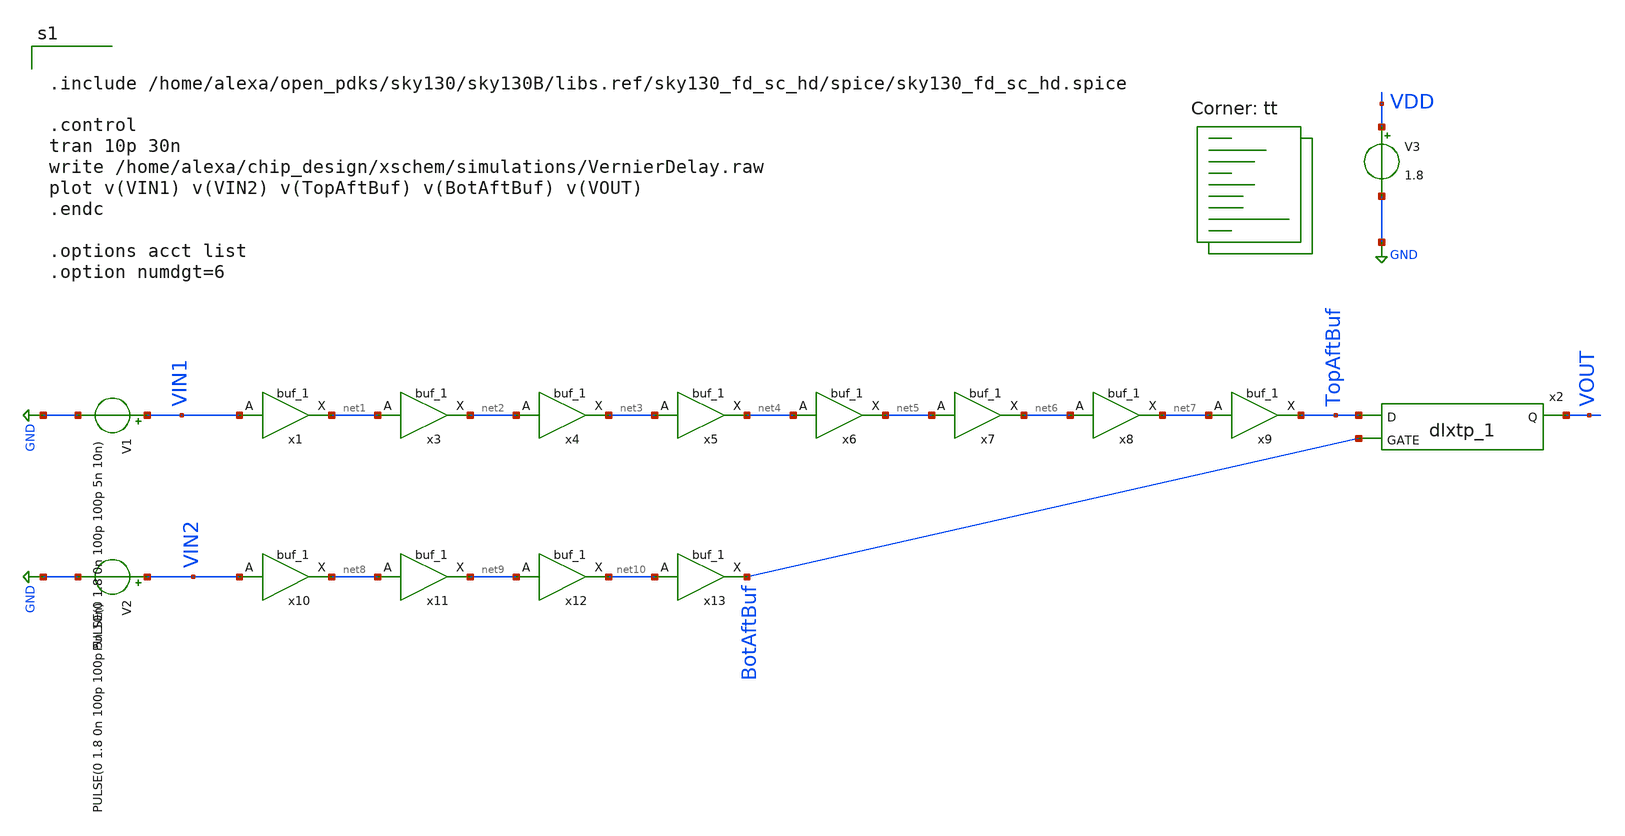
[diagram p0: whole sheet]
** sch_path: xschem/projects/SingleVernier.sch
* Copyright 2021 Stefan Frederik Schippers
* Licensed under the Apache License, Version 2.0 (the "License");
* you may not use this file except in compliance with the License.
* You may obtain a copy of the License at
* https://www.apache.org/licenses/LICENSE-2.0
* Unless required by applicable law or agreed to in writing, software
* distributed under the License is distributed on an "AS IS" BASIS,
* WITHOUT WARRANTIES OR CONDITIONS OF ANY KIND, either express or implied.
* See the License for the specific language governing permissions and
* limitations under the License.
**.subckt SingleVernier
x2 TopAftBuf BotAftBuf 0 0 VDD VDD VOUT sky130_fd_sc_hd__dlxtp_1
V1 VIN1 GND PULSE(0 1.8 0n 100p 100p 5n 10n)
V2 VIN2 GND PULSE(0 1.8 0n 100p 100p 5n 10n)
V3 VDD GND 1.8
x1 VIN1 0 0 VDD VDD net1 sky130_fd_sc_hd__buf_1
x3 net1 0 0 VDD VDD net2 sky130_fd_sc_hd__buf_1
x4 net2 0 0 VDD VDD net3 sky130_fd_sc_hd__buf_1
x5 net3 0 0 VDD VDD net4 sky130_fd_sc_hd__buf_1
x6 net4 0 0 VDD VDD net5 sky130_fd_sc_hd__buf_1
x7 net5 0 0 VDD VDD net6 sky130_fd_sc_hd__buf_1
x8 net6 0 0 VDD VDD net7 sky130_fd_sc_hd__buf_1
x9 net7 0 0 VDD VDD TopAftBuf sky130_fd_sc_hd__buf_1
x10 VIN2 0 0 VDD VDD net8 sky130_fd_sc_hd__buf_1
x11 net8 0 0 VDD VDD net9 sky130_fd_sc_hd__buf_1
x12 net9 0 0 VDD VDD net10 sky130_fd_sc_hd__buf_1
x13 net10 0 0 VDD VDD BotAftBuf sky130_fd_sc_hd__buf_1
**** begin user architecture code


.include /home/alexa/open_pdks/sky130/sky130B/libs.ref/sky130_fd_sc_hd/spice/sky130_fd_sc_hd.spice

.control
tran 10p 30n
write /home/alexa/chip_design/xschem/simulations/VernierDelay.raw
plot v(VIN1) v(VIN2) v(TopAftBuf) v(BotAftBuf) v(VOUT)
.endc

.options acct list
.option numdgt=6


.lib $::SKYWATER_MODELS/sky130.lib.spice tt
**** end user architecture code
**.ends
.GLOBAL GND
.end
